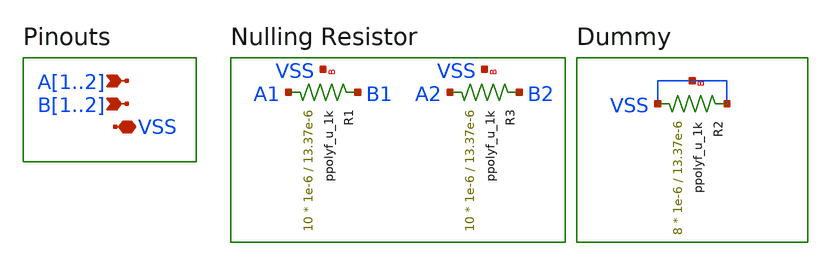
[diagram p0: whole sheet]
** sch_path: designs/libs/core_ota/differential_nulling_res/differential_nulling_res.sch
**.subckt differential_nulling_res VSS A1,A2 B1,B2
*.iopin VSS
*.ipin A1,A2
*.ipin B1,B2
XR2 VSS VSS VSS ppolyf_u_1k r_width=1e-6 r_length=13.37e-6 m=8
XR1 A1 B1 VSS ppolyf_u_1k r_width=1e-6 r_length=13.37e-6 m=10
XR3 A2 B2 VSS ppolyf_u_1k r_width=1e-6 r_length=13.37e-6 m=10
**.ends
.end
